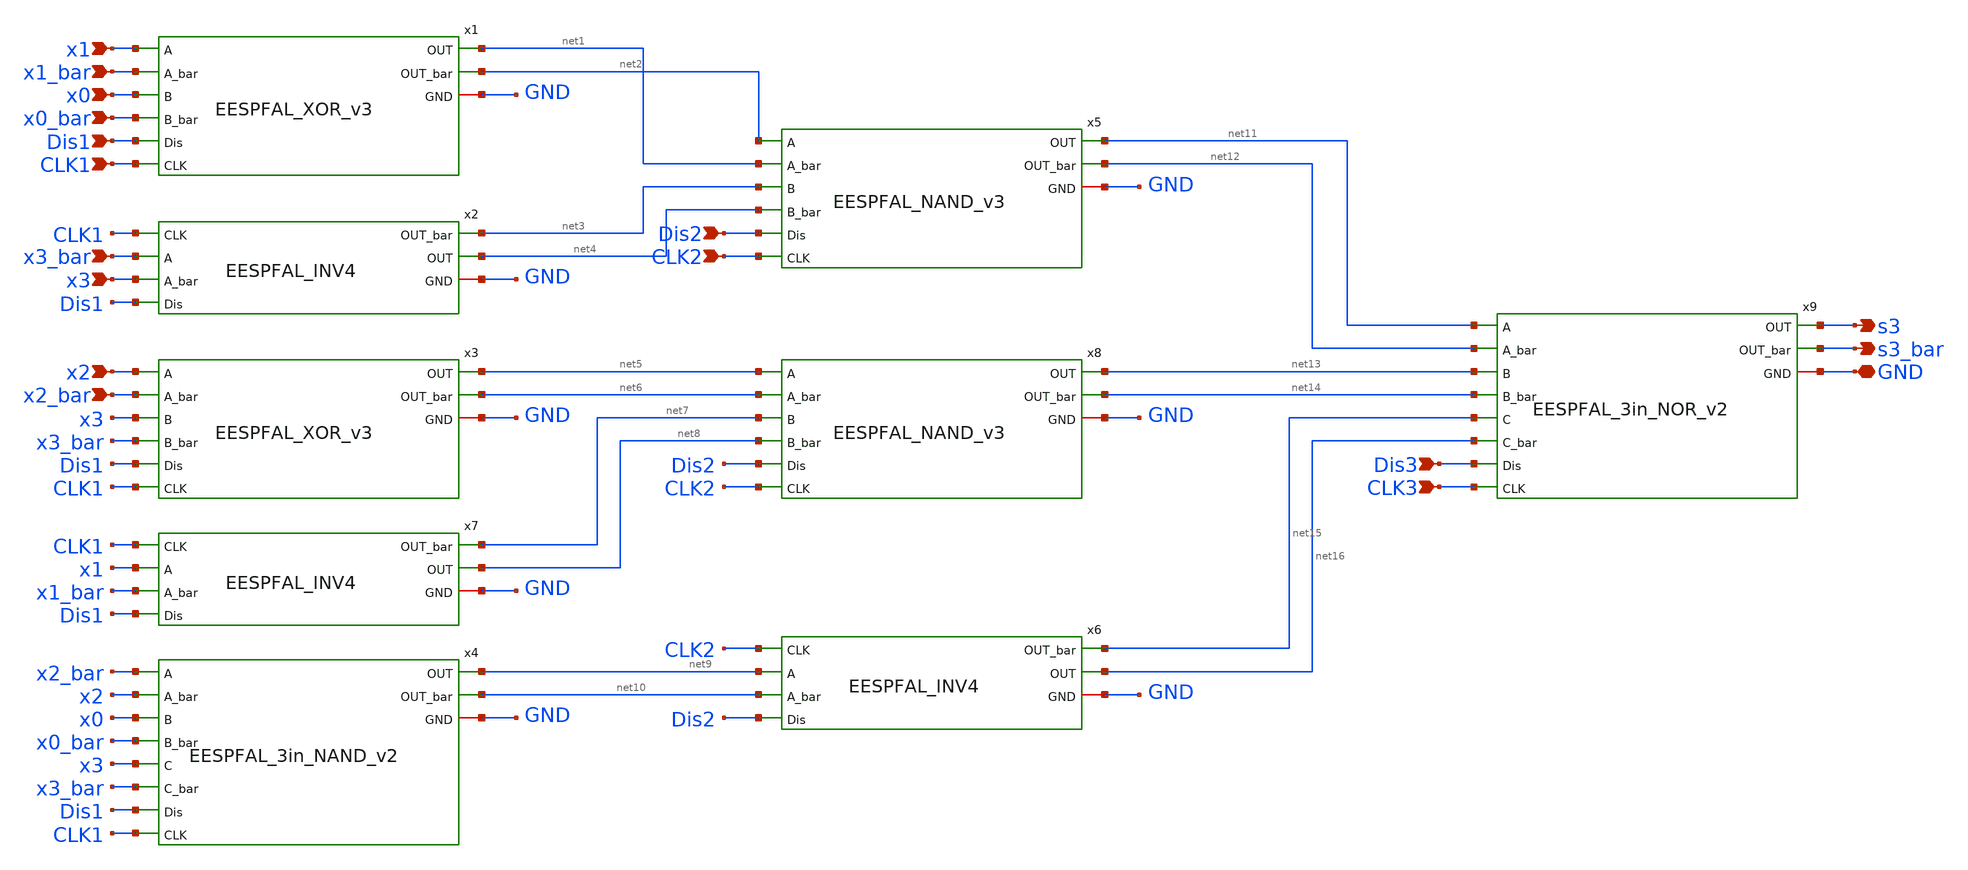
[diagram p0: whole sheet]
** sch_path: skywater_stuff/EESPFAL_s3_draft2.sch
**.subckt EESPFAL_s3_draft2 x0 x0_bar x1 x1_bar x2 x2_bar x3 x3_bar s3 s3_bar Dis1 Dis2 Dis3 GND
*+ CLK1 CLK2 CLK3
*.ipin x0
*.ipin x0_bar
*.ipin x1
*.ipin x1_bar
*.ipin x2
*.ipin x2_bar
*.ipin x3
*.ipin x3_bar
*.opin s3
*.opin s3_bar
*.ipin Dis1
*.ipin Dis2
*.ipin Dis3
*.iopin GND
*.ipin CLK1
*.ipin CLK2
*.ipin CLK3
x9 net11 net12 net13 net14 net15 net16 s3 s3_bar Dis3 GND CLK3 EESPFAL_3in_NOR_v2
x4 x2_bar x2 x0 x0_bar x3 x3_bar net9 net10 Dis1 GND CLK1 EESPFAL_3in_NAND_v2
x1 x1 x1_bar x0 x0_bar net1 net2 Dis1 GND CLK1 EESPFAL_XOR_v3
x2 x3_bar x3 net4 net3 Dis1 GND CLK1 EESPFAL_INV4
x3 x2 x2_bar x3 x3_bar net5 net6 Dis1 GND CLK1 EESPFAL_XOR_v3
x7 x1 x1_bar net8 net7 Dis1 GND CLK1 EESPFAL_INV4
x6 net9 net10 net16 net15 Dis2 GND CLK2 EESPFAL_INV4
x8 net5 net6 net7 net8 net13 net14 Dis2 GND CLK2 EESPFAL_NAND_v3
x5 net2 net1 net3 net4 net11 net12 Dis2 GND CLK2 EESPFAL_NAND_v3
**.ends
.end
